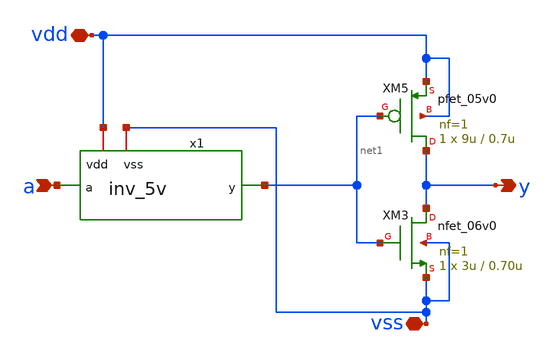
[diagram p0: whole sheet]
** sch_path: member_project/ice458/dynamic_comparator/xschem/out_buf_5v.sch
**.subckt out_buf_5v vdd vss a y
*.iopin vdd
*.iopin vss
*.ipin a
*.opin y
x1 vdd a net1 vss inv_5v
XM3 y net1 vss vss nfet_06v0 L=0.70u W=3u nf=1 ad='int((nf+1)/2) * W/nf * 0.18u' as='int((nf+2)/2) * W/nf * 0.18u'
+ pd='2*int((nf+1)/2) * (W/nf + 0.18u)' ps='2*int((nf+2)/2) * (W/nf + 0.18u)' nrd='0.18u / W' nrs='0.18u / W'
+ sa=0 sb=0 sd=0 m=1
XM5 y net1 vdd vdd pfet_05v0 L=0.7u W=9u nf=1 ad='int((nf+1)/2) * W/nf * 0.18u' as='int((nf+2)/2) * W/nf * 0.18u'
+ pd='2*int((nf+1)/2) * (W/nf + 0.18u)' ps='2*int((nf+2)/2) * (W/nf + 0.18u)' nrd='0.18u / W' nrs='0.18u / W'
+ sa=0 sb=0 sd=0 m=1
**.ends

* expanding   symbol:  inv_5v.sym # of pins=4
** sym_path: member_project/ice458/dynamic_comparator/xschem/inv_5v.sym
** sch_path: member_project/ice458/dynamic_comparator/xschem/inv_5v.sch
.subckt inv_5v vdd a y vss
*.iopin vdd
*.iopin vss
*.ipin a
*.opin y
XM3 y a vss vss nfet_06v0 L=0.70u W=1u nf=1 ad='int((nf+1)/2) * W/nf * 0.18u' as='int((nf+2)/2) * W/nf * 0.18u'
+ pd='2*int((nf+1)/2) * (W/nf + 0.18u)' ps='2*int((nf+2)/2) * (W/nf + 0.18u)' nrd='0.18u / W' nrs='0.18u / W'
+ sa=0 sb=0 sd=0 m=1
XM5 y a vdd vdd pfet_05v0 L=0.7u W=3u nf=1 ad='int((nf+1)/2) * W/nf * 0.18u' as='int((nf+2)/2) * W/nf * 0.18u'
+ pd='2*int((nf+1)/2) * (W/nf + 0.18u)' ps='2*int((nf+2)/2) * (W/nf + 0.18u)' nrd='0.18u / W' nrs='0.18u / W'
+ sa=0 sb=0 sd=0 m=1
.ends

.end
